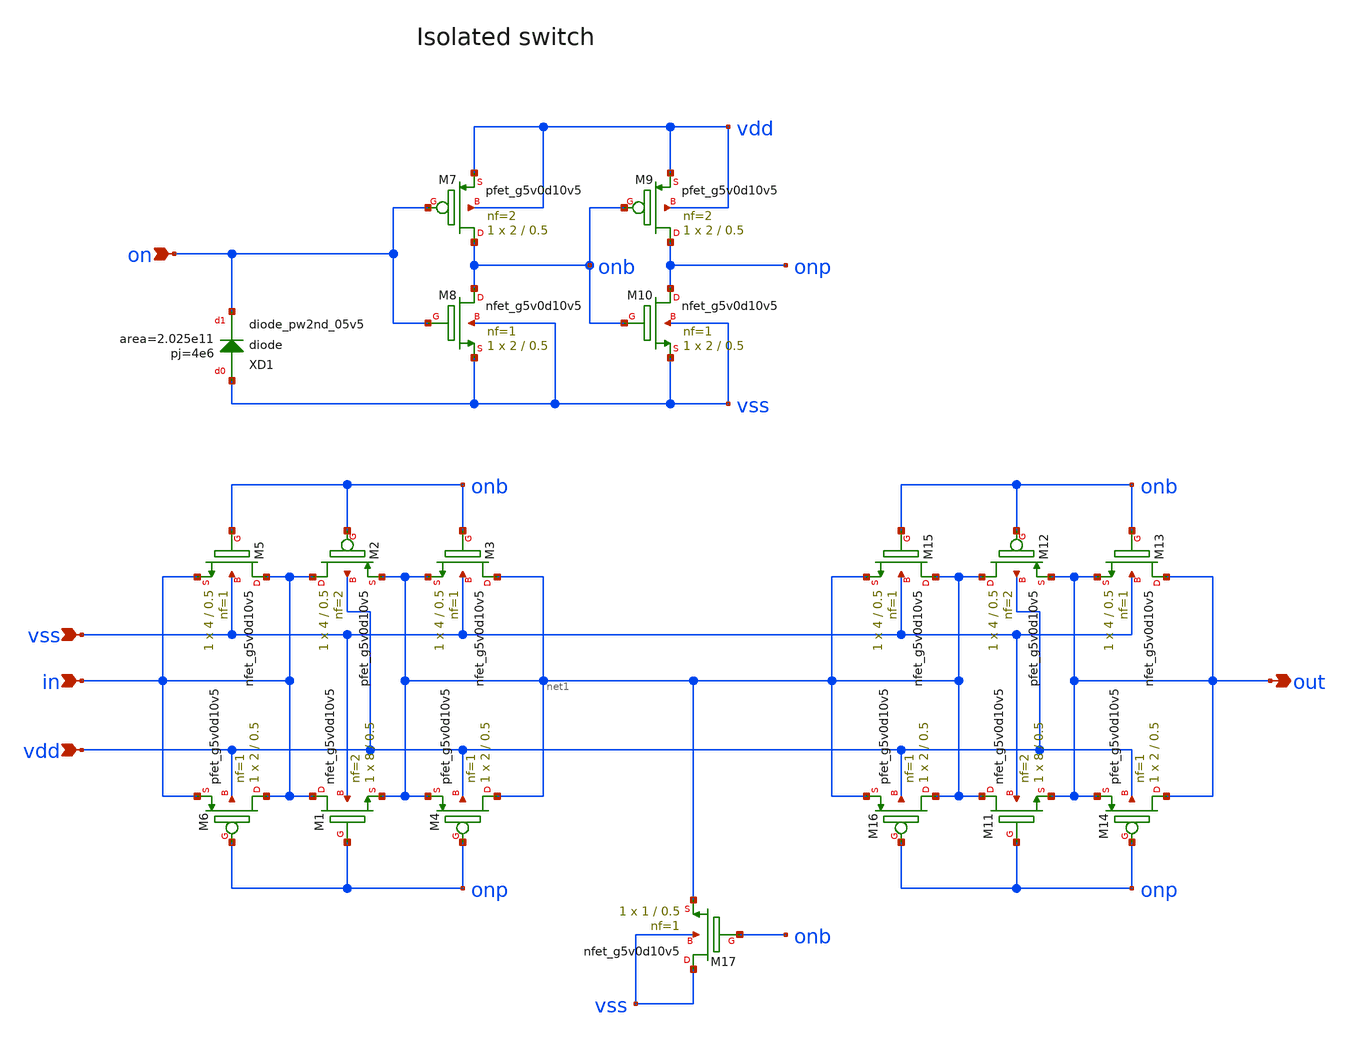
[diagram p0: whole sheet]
** sch_path: netlist/schematic/isolated_switch.sch
**.subckt isolated_switch in vss vdd on out
*.ipin in
*.ipin vss
*.ipin vdd
*.ipin on
*.opin out
XM1 in onp net1 vss sky130_fd_pr__nfet_g5v0d10v5 L=0.5 W=8 nf=2 ad='int((nf+1)/2) * W/nf * 0.29' as='int((nf+2)/2) * W/nf * 0.29'
+ pd='2*int((nf+1)/2) * (W/nf + 0.29)' ps='2*int((nf+2)/2) * (W/nf + 0.29)' nrd='0.29 / W' nrs='0.29 / W'
+ sa=0 sb=0 sd=0 mult=1 m=1
XM2 in onb net1 vdd sky130_fd_pr__pfet_g5v0d10v5 L=0.5 W=4 nf=2 ad='int((nf+1)/2) * W/nf * 0.29' as='int((nf+2)/2) * W/nf * 0.29'
+ pd='2*int((nf+1)/2) * (W/nf + 0.29)' ps='2*int((nf+2)/2) * (W/nf + 0.29)' nrd='0.29 / W' nrs='0.29 / W'
+ sa=0 sb=0 sd=0 mult=1 m=1
XM3 net1 onb net1 vss sky130_fd_pr__nfet_g5v0d10v5 L=0.5 W=4 nf=1 ad='int((nf+1)/2) * W/nf * 0.29' as='int((nf+2)/2) * W/nf * 0.29'
+ pd='2*int((nf+1)/2) * (W/nf + 0.29)' ps='2*int((nf+2)/2) * (W/nf + 0.29)' nrd='0.29 / W' nrs='0.29 / W'
+ sa=0 sb=0 sd=0 mult=1 m=1
XM4 net1 onp net1 vdd sky130_fd_pr__pfet_g5v0d10v5 L=0.5 W=2 nf=1 ad='int((nf+1)/2) * W/nf * 0.29' as='int((nf+2)/2) * W/nf * 0.29'
+ pd='2*int((nf+1)/2) * (W/nf + 0.29)' ps='2*int((nf+2)/2) * (W/nf + 0.29)' nrd='0.29 / W' nrs='0.29 / W'
+ sa=0 sb=0 sd=0 mult=1 m=1
XM5 in onb in vss sky130_fd_pr__nfet_g5v0d10v5 L=0.5 W=4 nf=1 ad='int((nf+1)/2) * W/nf * 0.29' as='int((nf+2)/2) * W/nf * 0.29'
+ pd='2*int((nf+1)/2) * (W/nf + 0.29)' ps='2*int((nf+2)/2) * (W/nf + 0.29)' nrd='0.29 / W' nrs='0.29 / W'
+ sa=0 sb=0 sd=0 mult=1 m=1
XM6 in onp in vdd sky130_fd_pr__pfet_g5v0d10v5 L=0.5 W=2 nf=1 ad='int((nf+1)/2) * W/nf * 0.29' as='int((nf+2)/2) * W/nf * 0.29'
+ pd='2*int((nf+1)/2) * (W/nf + 0.29)' ps='2*int((nf+2)/2) * (W/nf + 0.29)' nrd='0.29 / W' nrs='0.29 / W'
+ sa=0 sb=0 sd=0 mult=1 m=1
XM7 onb on vdd vdd sky130_fd_pr__pfet_g5v0d10v5 L=0.5 W=2 nf=2 ad='int((nf+1)/2) * W/nf * 0.29' as='int((nf+2)/2) * W/nf * 0.29'
+ pd='2*int((nf+1)/2) * (W/nf + 0.29)' ps='2*int((nf+2)/2) * (W/nf + 0.29)' nrd='0.29 / W' nrs='0.29 / W'
+ sa=0 sb=0 sd=0 mult=1 m=1
XM8 onb on vss vss sky130_fd_pr__nfet_g5v0d10v5 L=0.5 W=2 nf=1 ad='int((nf+1)/2) * W/nf * 0.29' as='int((nf+2)/2) * W/nf * 0.29'
+ pd='2*int((nf+1)/2) * (W/nf + 0.29)' ps='2*int((nf+2)/2) * (W/nf + 0.29)' nrd='0.29 / W' nrs='0.29 / W'
+ sa=0 sb=0 sd=0 mult=1 m=1
XM9 onp onb vdd vdd sky130_fd_pr__pfet_g5v0d10v5 L=0.5 W=2 nf=2 ad='int((nf+1)/2) * W/nf * 0.29' as='int((nf+2)/2) * W/nf * 0.29'
+ pd='2*int((nf+1)/2) * (W/nf + 0.29)' ps='2*int((nf+2)/2) * (W/nf + 0.29)' nrd='0.29 / W' nrs='0.29 / W'
+ sa=0 sb=0 sd=0 mult=1 m=1
XM10 onp onb vss vss sky130_fd_pr__nfet_g5v0d10v5 L=0.5 W=2 nf=1 ad='int((nf+1)/2) * W/nf * 0.29' as='int((nf+2)/2) * W/nf * 0.29'
+ pd='2*int((nf+1)/2) * (W/nf + 0.29)' ps='2*int((nf+2)/2) * (W/nf + 0.29)' nrd='0.29 / W' nrs='0.29 / W'
+ sa=0 sb=0 sd=0 mult=1 m=1
XXD1 vss on sky130_fd_pr__diode_pw2nd_05v5 area=2.025e11 pj=4e6
XM11 net1 onp out vss sky130_fd_pr__nfet_g5v0d10v5 L=0.5 W=8 nf=2 ad='int((nf+1)/2) * W/nf * 0.29' as='int((nf+2)/2) * W/nf * 0.29'
+ pd='2*int((nf+1)/2) * (W/nf + 0.29)' ps='2*int((nf+2)/2) * (W/nf + 0.29)' nrd='0.29 / W' nrs='0.29 / W'
+ sa=0 sb=0 sd=0 mult=1 m=1
XM12 net1 onb out vdd sky130_fd_pr__pfet_g5v0d10v5 L=0.5 W=4 nf=2 ad='int((nf+1)/2) * W/nf * 0.29' as='int((nf+2)/2) * W/nf * 0.29'
+ pd='2*int((nf+1)/2) * (W/nf + 0.29)' ps='2*int((nf+2)/2) * (W/nf + 0.29)' nrd='0.29 / W' nrs='0.29 / W'
+ sa=0 sb=0 sd=0 mult=1 m=1
XM13 out onb out vss sky130_fd_pr__nfet_g5v0d10v5 L=0.5 W=4 nf=1 ad='int((nf+1)/2) * W/nf * 0.29' as='int((nf+2)/2) * W/nf * 0.29'
+ pd='2*int((nf+1)/2) * (W/nf + 0.29)' ps='2*int((nf+2)/2) * (W/nf + 0.29)' nrd='0.29 / W' nrs='0.29 / W'
+ sa=0 sb=0 sd=0 mult=1 m=1
XM14 out onp out vdd sky130_fd_pr__pfet_g5v0d10v5 L=0.5 W=2 nf=1 ad='int((nf+1)/2) * W/nf * 0.29' as='int((nf+2)/2) * W/nf * 0.29'
+ pd='2*int((nf+1)/2) * (W/nf + 0.29)' ps='2*int((nf+2)/2) * (W/nf + 0.29)' nrd='0.29 / W' nrs='0.29 / W'
+ sa=0 sb=0 sd=0 mult=1 m=1
XM15 net1 onb net1 vss sky130_fd_pr__nfet_g5v0d10v5 L=0.5 W=4 nf=1 ad='int((nf+1)/2) * W/nf * 0.29' as='int((nf+2)/2) * W/nf * 0.29'
+ pd='2*int((nf+1)/2) * (W/nf + 0.29)' ps='2*int((nf+2)/2) * (W/nf + 0.29)' nrd='0.29 / W' nrs='0.29 / W'
+ sa=0 sb=0 sd=0 mult=1 m=1
XM16 net1 onp net1 vdd sky130_fd_pr__pfet_g5v0d10v5 L=0.5 W=2 nf=1 ad='int((nf+1)/2) * W/nf * 0.29' as='int((nf+2)/2) * W/nf * 0.29'
+ pd='2*int((nf+1)/2) * (W/nf + 0.29)' ps='2*int((nf+2)/2) * (W/nf + 0.29)' nrd='0.29 / W' nrs='0.29 / W'
+ sa=0 sb=0 sd=0 mult=1 m=1
XM17 vss onb net1 vss sky130_fd_pr__nfet_g5v0d10v5 L=0.5 W=1 nf=1 ad='int((nf+1)/2) * W/nf * 0.29' as='int((nf+2)/2) * W/nf * 0.29'
+ pd='2*int((nf+1)/2) * (W/nf + 0.29)' ps='2*int((nf+2)/2) * (W/nf + 0.29)' nrd='0.29 / W' nrs='0.29 / W'
+ sa=0 sb=0 sd=0 mult=1 m=1
**.ends
.end
